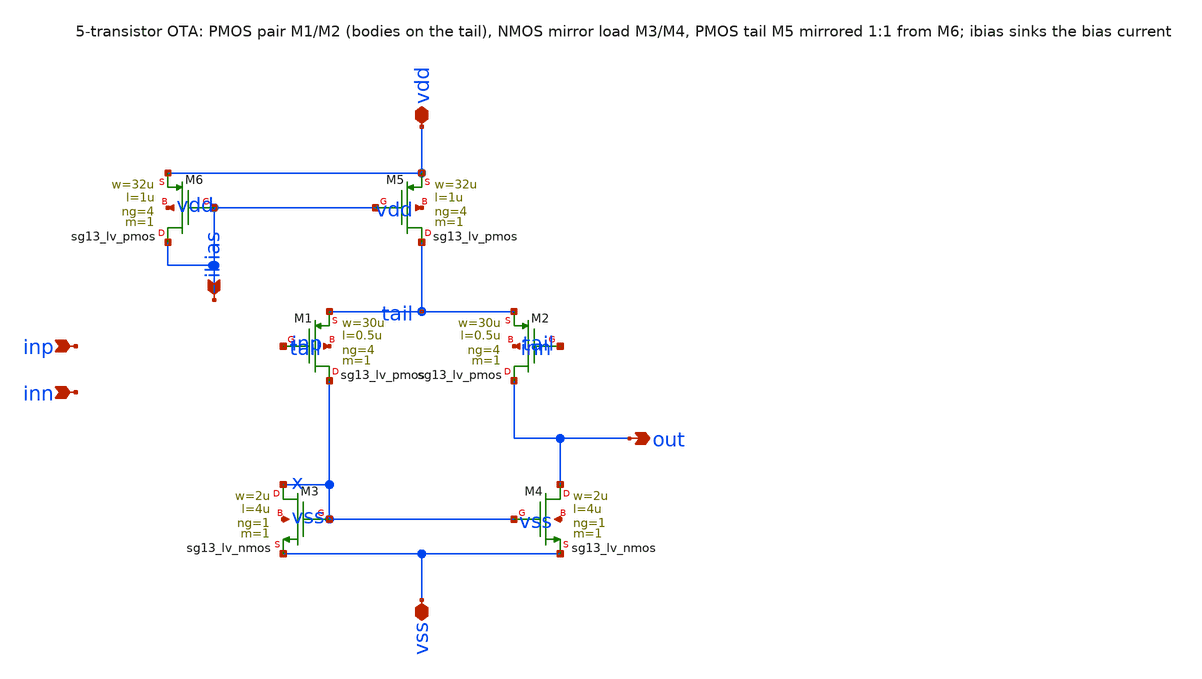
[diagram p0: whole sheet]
** sch_path: cdept-gui/tutorials/start/ota-sch/libs/work/ota5t/schematic/ota5t.sch
**.subckt ota5t inp inn ibias out vdd vss
*.ipin inp
*.ipin inn
*.ipin ibias
*.opin out
*.iopin vdd
*.iopin vss
XM5 tail ibias vdd vdd sg13_lv_pmos w=32u l=1u ng=4 m=1 mm_ok=1
XM6 ibias ibias vdd vdd sg13_lv_pmos w=32u l=1u ng=4 m=1 mm_ok=1
XM1 x inp tail tail sg13_lv_pmos w=30u l=0.5u ng=4 m=1 mm_ok=1
XM2 out inn tail tail sg13_lv_pmos w=30u l=0.5u ng=4 m=1 mm_ok=1
XM3 x x vss vss sg13_lv_nmos w=2u l=4u ng=1 m=1 mm_ok=1
XM4 out x vss vss sg13_lv_nmos w=2u l=4u ng=1 m=1 mm_ok=1
**.ends
.end
